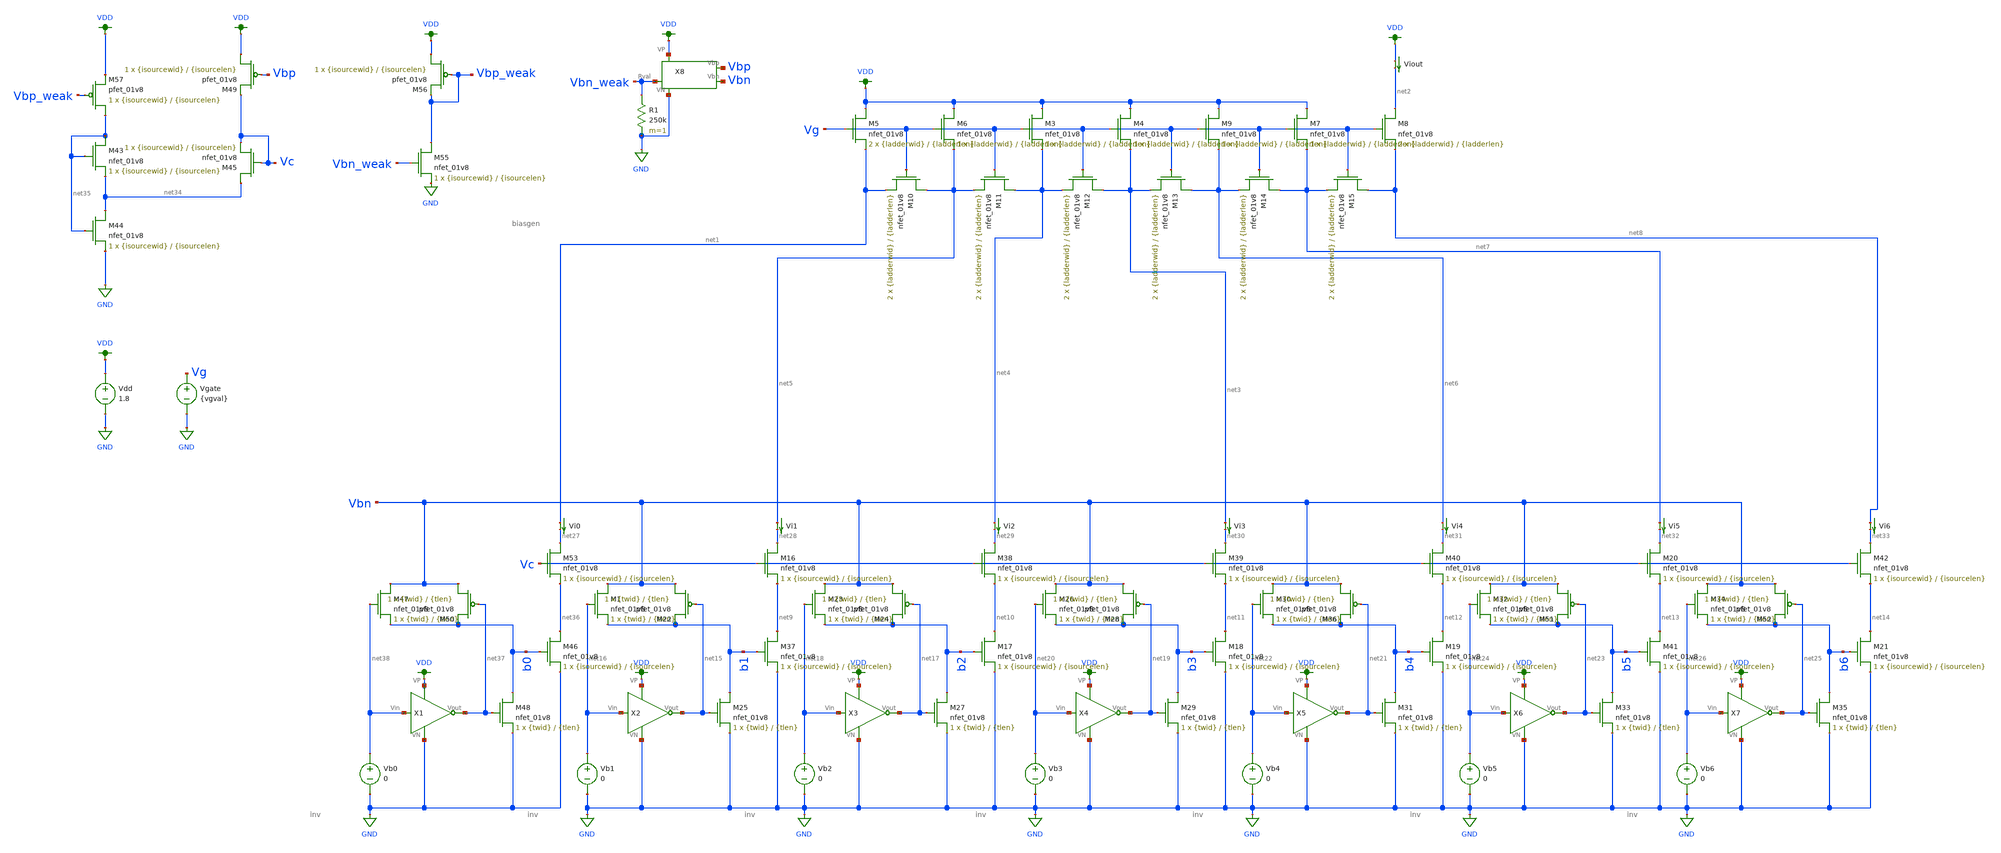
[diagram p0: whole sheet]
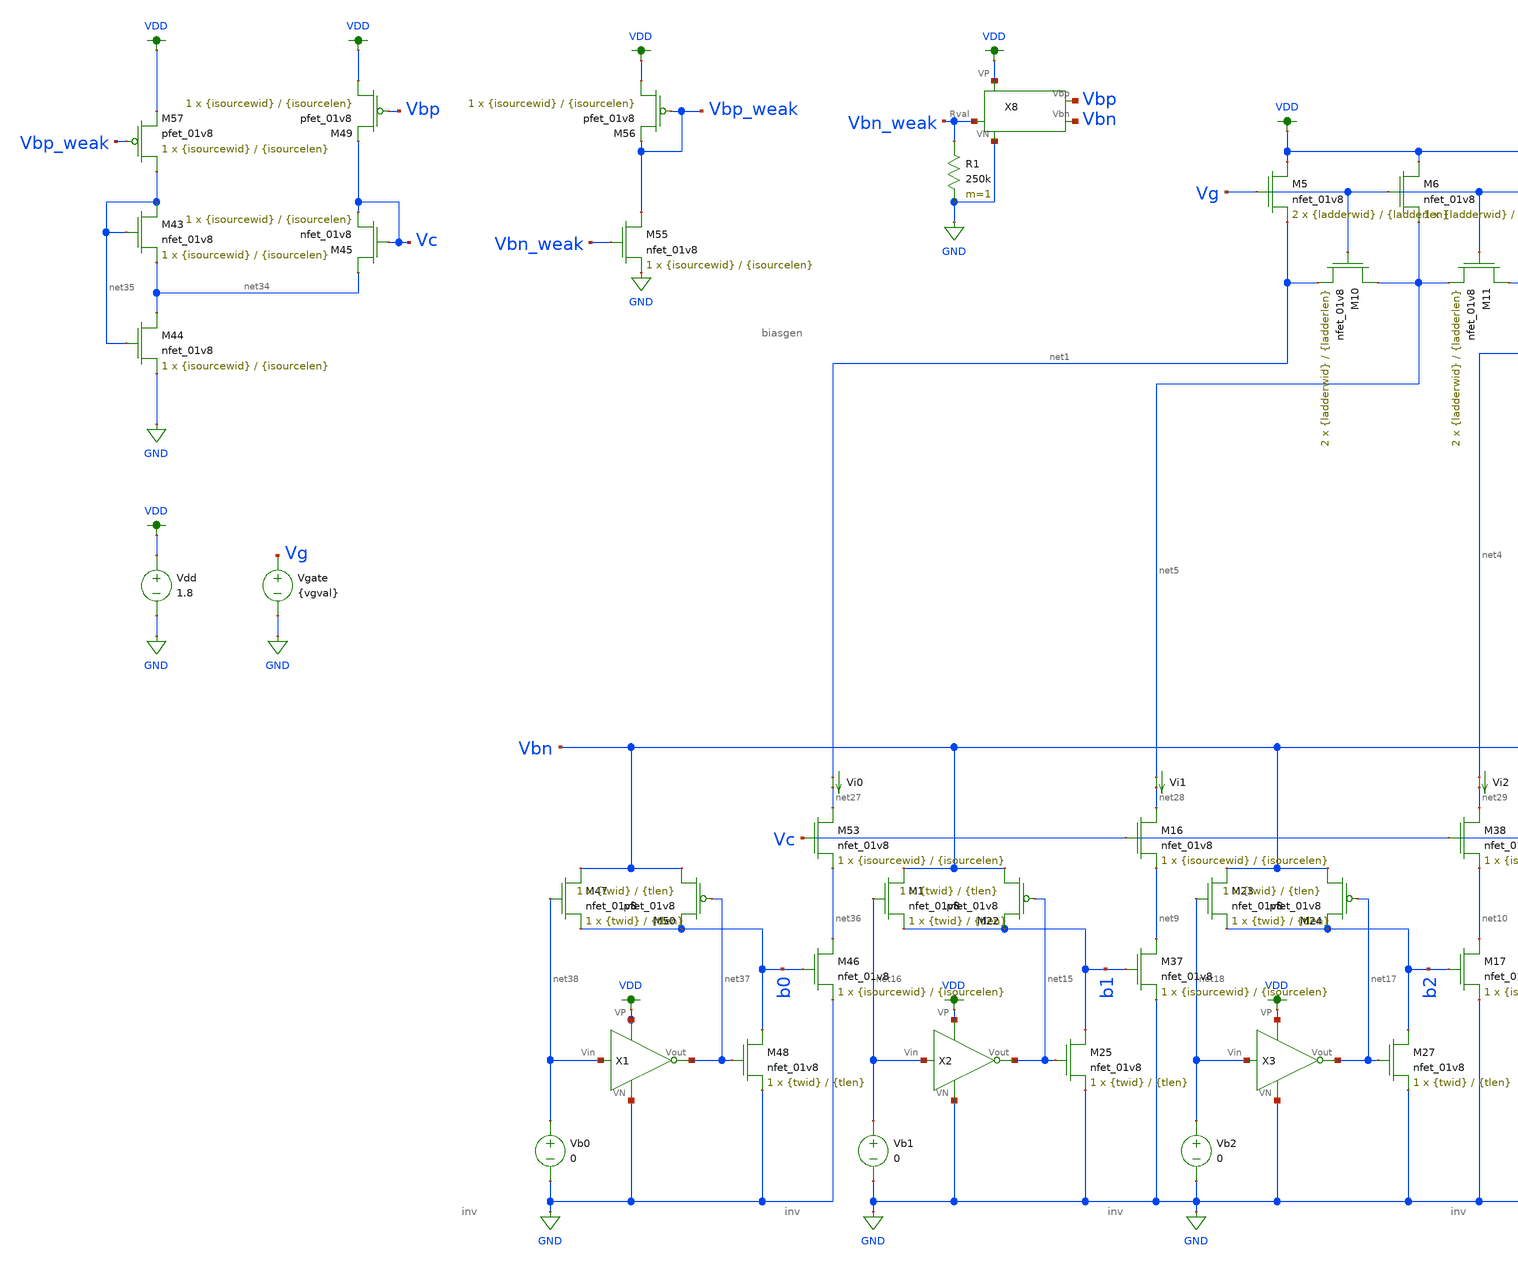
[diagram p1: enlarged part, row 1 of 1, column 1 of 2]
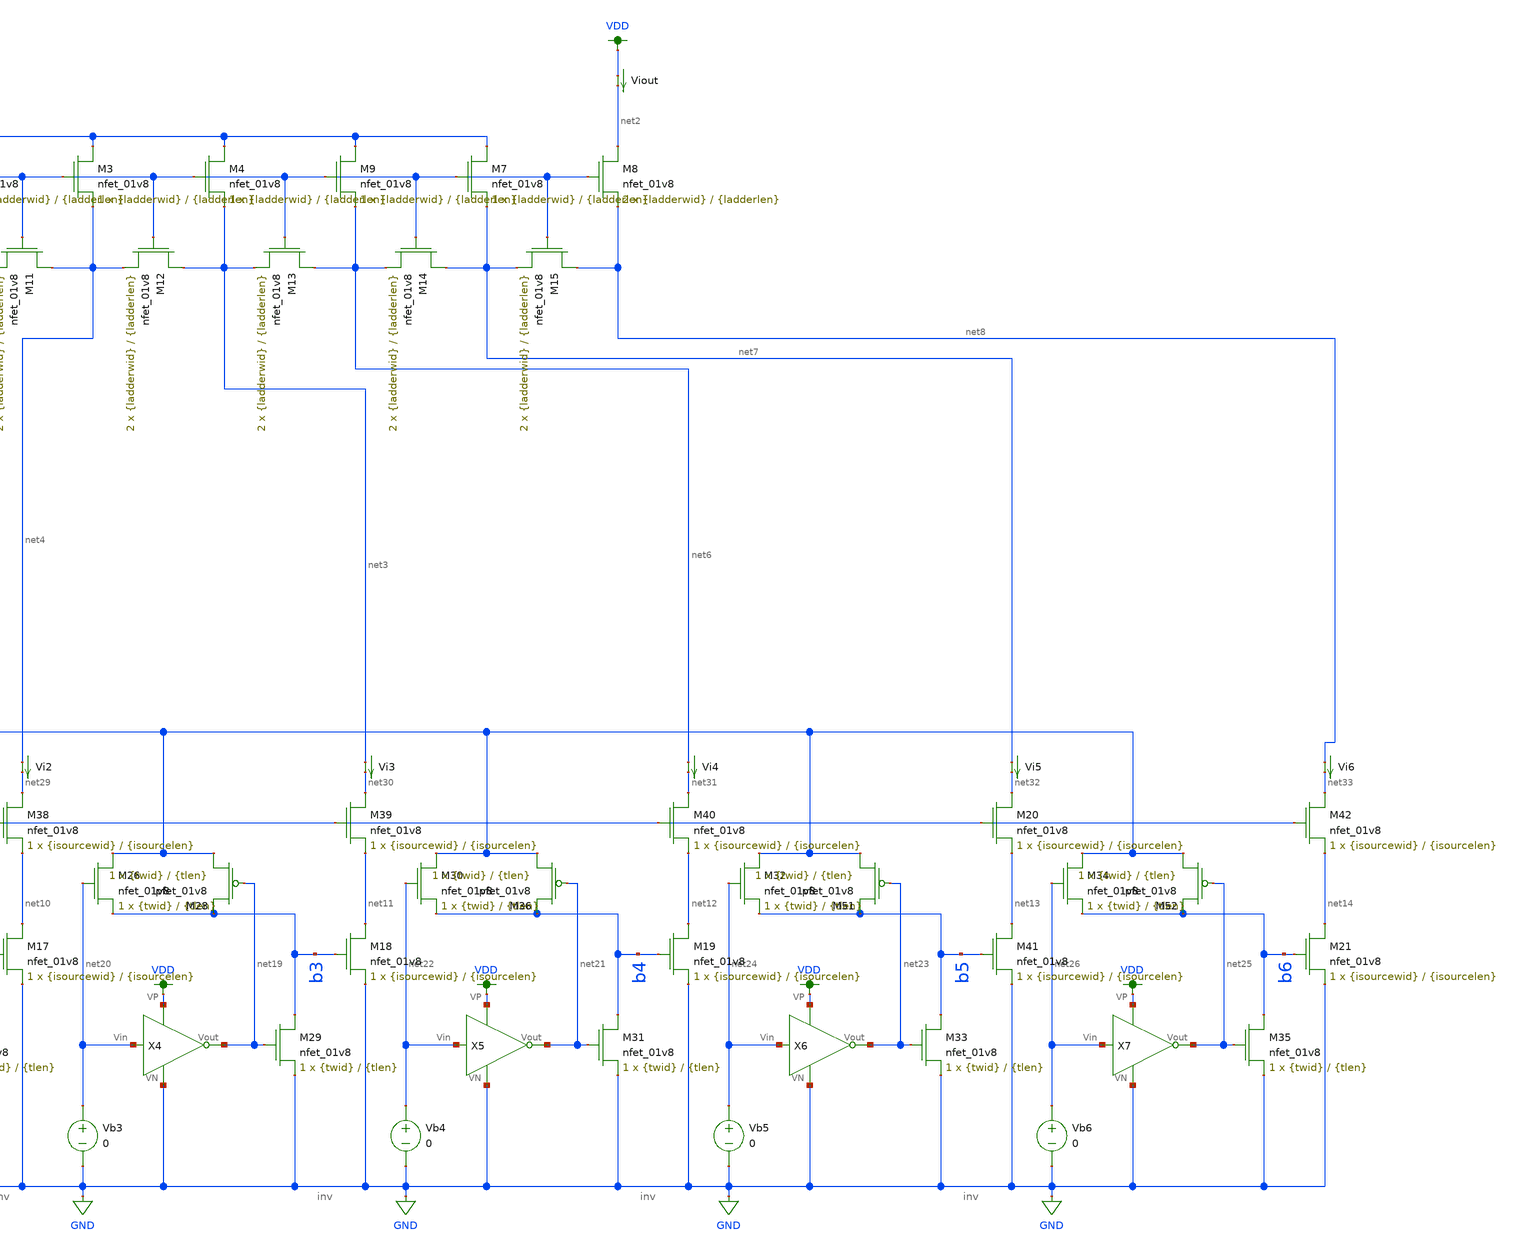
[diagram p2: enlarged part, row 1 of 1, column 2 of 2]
** sch_path: prelim-files/testing.sch
**.subckt testing
Vdd VDD GND 1.8
Vi0 net1 net27 0
.save i(vi0)
XM5 VDD Vg net1 GND sky130_fd_pr__nfet_01v8 L={ladderlen} W={ladderwid} nf=1 ad='int((nf+1)/2) * W/nf * 0.29'
+ as='int((nf+2)/2) * W/nf * 0.29' pd='2*int((nf+1)/2) * (W/nf + 0.29)' ps='2*int((nf+2)/2) * (W/nf + 0.29)'
+ nrd='0.29 / W' nrs='0.29 / W' sa=0 sb=0 sd=0 mult=2 m=2
XM6 VDD Vg net5 GND sky130_fd_pr__nfet_01v8 L={ladderlen} W={ladderwid} nf=1 ad='int((nf+1)/2) * W/nf * 0.29'
+ as='int((nf+2)/2) * W/nf * 0.29' pd='2*int((nf+1)/2) * (W/nf + 0.29)' ps='2*int((nf+2)/2) * (W/nf + 0.29)'
+ nrd='0.29 / W' nrs='0.29 / W' sa=0 sb=0 sd=0 mult=1 m=1
Viout VDD net2 0
.save i(viout)
Vb1 net16 GND 0
Vb2 net18 GND 0
Vgate Vg GND {vgval}
Vi1 net5 net28 0
.save i(vi1)
Vi2 net4 net29 0
.save i(vi2)
Vb3 net20 GND 0
Vi3 net3 net30 0
.save i(vi3)
Vb4 net22 GND 0
Vi4 net6 net31 0
.save i(vi4)
Vb5 net24 GND 0
Vi5 net7 net32 0
.save i(vi5)
Vb6 net26 GND 0
Vi6 net8 net33 0
.save i(vi6)
XM25 b1 net15 GND GND sky130_fd_pr__nfet_01v8 L={tlen} W={twid} nf=1 ad='int((nf+1)/2) * W/nf * 0.29'
+ as='int((nf+2)/2) * W/nf * 0.29' pd='2*int((nf+1)/2) * (W/nf + 0.29)' ps='2*int((nf+2)/2) * (W/nf + 0.29)'
+ nrd='0.29 / W' nrs='0.29 / W' sa=0 sb=0 sd=0 mult=1 m=1
XM27 b2 net17 GND GND sky130_fd_pr__nfet_01v8 L={tlen} W={twid} nf=1 ad='int((nf+1)/2) * W/nf * 0.29'
+ as='int((nf+2)/2) * W/nf * 0.29' pd='2*int((nf+1)/2) * (W/nf + 0.29)' ps='2*int((nf+2)/2) * (W/nf + 0.29)'
+ nrd='0.29 / W' nrs='0.29 / W' sa=0 sb=0 sd=0 mult=1 m=1
XM29 b3 net19 GND GND sky130_fd_pr__nfet_01v8 L={tlen} W={twid} nf=1 ad='int((nf+1)/2) * W/nf * 0.29'
+ as='int((nf+2)/2) * W/nf * 0.29' pd='2*int((nf+1)/2) * (W/nf + 0.29)' ps='2*int((nf+2)/2) * (W/nf + 0.29)'
+ nrd='0.29 / W' nrs='0.29 / W' sa=0 sb=0 sd=0 mult=1 m=1
XM31 b4 net21 GND GND sky130_fd_pr__nfet_01v8 L={tlen} W={twid} nf=1 ad='int((nf+1)/2) * W/nf * 0.29'
+ as='int((nf+2)/2) * W/nf * 0.29' pd='2*int((nf+1)/2) * (W/nf + 0.29)' ps='2*int((nf+2)/2) * (W/nf + 0.29)'
+ nrd='0.29 / W' nrs='0.29 / W' sa=0 sb=0 sd=0 mult=1 m=1
XM33 b5 net23 GND GND sky130_fd_pr__nfet_01v8 L={tlen} W={twid} nf=1 ad='int((nf+1)/2) * W/nf * 0.29'
+ as='int((nf+2)/2) * W/nf * 0.29' pd='2*int((nf+1)/2) * (W/nf + 0.29)' ps='2*int((nf+2)/2) * (W/nf + 0.29)'
+ nrd='0.29 / W' nrs='0.29 / W' sa=0 sb=0 sd=0 mult=1 m=1
XM35 b6 net25 GND GND sky130_fd_pr__nfet_01v8 L={tlen} W={twid} nf=1 ad='int((nf+1)/2) * W/nf * 0.29'
+ as='int((nf+2)/2) * W/nf * 0.29' pd='2*int((nf+1)/2) * (W/nf + 0.29)' ps='2*int((nf+2)/2) * (W/nf + 0.29)'
+ nrd='0.29 / W' nrs='0.29 / W' sa=0 sb=0 sd=0 mult=1 m=1
XM43 net35 net35 net34 GND sky130_fd_pr__nfet_01v8 L={isourcelen} W={isourcewid} nf=1 ad='int((nf+1)/2) * W/nf * 0.29'
+ as='int((nf+2)/2) * W/nf * 0.29' pd='2*int((nf+1)/2) * (W/nf + 0.29)' ps='2*int((nf+2)/2) * (W/nf + 0.29)'
+ nrd='0.29 / W' nrs='0.29 / W' sa=0 sb=0 sd=0 mult=1 m=1
XM44 net34 net35 GND GND sky130_fd_pr__nfet_01v8 L={isourcelen} W={isourcewid} nf=1 ad='int((nf+1)/2) * W/nf * 0.29'
+ as='int((nf+2)/2) * W/nf * 0.29' pd='2*int((nf+1)/2) * (W/nf + 0.29)' ps='2*int((nf+2)/2) * (W/nf + 0.29)'
+ nrd='0.29 / W' nrs='0.29 / W' sa=0 sb=0 sd=0 mult=1 m=1
XM45 net34 Vc Vc GND sky130_fd_pr__nfet_01v8 L={isourcelen} W={isourcewid} nf=1 ad='int((nf+1)/2) * W/nf * 0.29'
+ as='int((nf+2)/2) * W/nf * 0.29' pd='2*int((nf+1)/2) * (W/nf + 0.29)' ps='2*int((nf+2)/2) * (W/nf + 0.29)'
+ nrd='0.29 / W' nrs='0.29 / W' sa=0 sb=0 sd=0 mult=1 m=1
Vb0 net38 GND 0
XM47 Vbn net38 b0 GND sky130_fd_pr__nfet_01v8 L={tlen} W={twid} nf=1 ad='int((nf+1)/2) * W/nf * 0.29'
+ as='int((nf+2)/2) * W/nf * 0.29' pd='2*int((nf+1)/2) * (W/nf + 0.29)' ps='2*int((nf+2)/2) * (W/nf + 0.29)'
+ nrd='0.29 / W' nrs='0.29 / W' sa=0 sb=0 sd=0 mult=1 m=1
XM48 b0 net37 GND GND sky130_fd_pr__nfet_01v8 L={tlen} W={twid} nf=1 ad='int((nf+1)/2) * W/nf * 0.29'
+ as='int((nf+2)/2) * W/nf * 0.29' pd='2*int((nf+1)/2) * (W/nf + 0.29)' ps='2*int((nf+2)/2) * (W/nf + 0.29)'
+ nrd='0.29 / W' nrs='0.29 / W' sa=0 sb=0 sd=0 mult=1 m=1
XM50 Vbn net37 b0 VDD sky130_fd_pr__pfet_01v8 L={tlen} W={twid} nf=1 ad='int((nf+1)/2) * W/nf * 0.29'
+ as='int((nf+2)/2) * W/nf * 0.29' pd='2*int((nf+1)/2) * (W/nf + 0.29)' ps='2*int((nf+2)/2) * (W/nf + 0.29)'
+ nrd='0.29 / W' nrs='0.29 / W' sa=0 sb=0 sd=0 mult=1 m=1
XM1 Vbn net16 b1 GND sky130_fd_pr__nfet_01v8 L={tlen} W={twid} nf=1 ad='int((nf+1)/2) * W/nf * 0.29'
+ as='int((nf+2)/2) * W/nf * 0.29' pd='2*int((nf+1)/2) * (W/nf + 0.29)' ps='2*int((nf+2)/2) * (W/nf + 0.29)'
+ nrd='0.29 / W' nrs='0.29 / W' sa=0 sb=0 sd=0 mult=1 m=1
XM22 Vbn net15 b1 VDD sky130_fd_pr__pfet_01v8 L={tlen} W={twid} nf=1 ad='int((nf+1)/2) * W/nf * 0.29'
+ as='int((nf+2)/2) * W/nf * 0.29' pd='2*int((nf+1)/2) * (W/nf + 0.29)' ps='2*int((nf+2)/2) * (W/nf + 0.29)'
+ nrd='0.29 / W' nrs='0.29 / W' sa=0 sb=0 sd=0 mult=1 m=1
XM23 Vbn net18 b2 GND sky130_fd_pr__nfet_01v8 L={tlen} W={twid} nf=1 ad='int((nf+1)/2) * W/nf * 0.29'
+ as='int((nf+2)/2) * W/nf * 0.29' pd='2*int((nf+1)/2) * (W/nf + 0.29)' ps='2*int((nf+2)/2) * (W/nf + 0.29)'
+ nrd='0.29 / W' nrs='0.29 / W' sa=0 sb=0 sd=0 mult=1 m=1
XM24 Vbn net17 b2 VDD sky130_fd_pr__pfet_01v8 L={tlen} W={twid} nf=1 ad='int((nf+1)/2) * W/nf * 0.29'
+ as='int((nf+2)/2) * W/nf * 0.29' pd='2*int((nf+1)/2) * (W/nf + 0.29)' ps='2*int((nf+2)/2) * (W/nf + 0.29)'
+ nrd='0.29 / W' nrs='0.29 / W' sa=0 sb=0 sd=0 mult=1 m=1
XM26 Vbn net20 b3 GND sky130_fd_pr__nfet_01v8 L={tlen} W={twid} nf=1 ad='int((nf+1)/2) * W/nf * 0.29'
+ as='int((nf+2)/2) * W/nf * 0.29' pd='2*int((nf+1)/2) * (W/nf + 0.29)' ps='2*int((nf+2)/2) * (W/nf + 0.29)'
+ nrd='0.29 / W' nrs='0.29 / W' sa=0 sb=0 sd=0 mult=1 m=1
XM28 Vbn net19 b3 VDD sky130_fd_pr__pfet_01v8 L={tlen} W={twid} nf=1 ad='int((nf+1)/2) * W/nf * 0.29'
+ as='int((nf+2)/2) * W/nf * 0.29' pd='2*int((nf+1)/2) * (W/nf + 0.29)' ps='2*int((nf+2)/2) * (W/nf + 0.29)'
+ nrd='0.29 / W' nrs='0.29 / W' sa=0 sb=0 sd=0 mult=1 m=1
XM30 Vbn net22 b4 GND sky130_fd_pr__nfet_01v8 L={tlen} W={twid} nf=1 ad='int((nf+1)/2) * W/nf * 0.29'
+ as='int((nf+2)/2) * W/nf * 0.29' pd='2*int((nf+1)/2) * (W/nf + 0.29)' ps='2*int((nf+2)/2) * (W/nf + 0.29)'
+ nrd='0.29 / W' nrs='0.29 / W' sa=0 sb=0 sd=0 mult=1 m=1
XM36 Vbn net21 b4 VDD sky130_fd_pr__pfet_01v8 L={tlen} W={twid} nf=1 ad='int((nf+1)/2) * W/nf * 0.29'
+ as='int((nf+2)/2) * W/nf * 0.29' pd='2*int((nf+1)/2) * (W/nf + 0.29)' ps='2*int((nf+2)/2) * (W/nf + 0.29)'
+ nrd='0.29 / W' nrs='0.29 / W' sa=0 sb=0 sd=0 mult=1 m=1
XM32 Vbn net24 b5 GND sky130_fd_pr__nfet_01v8 L={tlen} W={twid} nf=1 ad='int((nf+1)/2) * W/nf * 0.29'
+ as='int((nf+2)/2) * W/nf * 0.29' pd='2*int((nf+1)/2) * (W/nf + 0.29)' ps='2*int((nf+2)/2) * (W/nf + 0.29)'
+ nrd='0.29 / W' nrs='0.29 / W' sa=0 sb=0 sd=0 mult=1 m=1
XM51 Vbn net23 b5 VDD sky130_fd_pr__pfet_01v8 L={tlen} W={twid} nf=1 ad='int((nf+1)/2) * W/nf * 0.29'
+ as='int((nf+2)/2) * W/nf * 0.29' pd='2*int((nf+1)/2) * (W/nf + 0.29)' ps='2*int((nf+2)/2) * (W/nf + 0.29)'
+ nrd='0.29 / W' nrs='0.29 / W' sa=0 sb=0 sd=0 mult=1 m=1
XM34 Vbn net26 b6 GND sky130_fd_pr__nfet_01v8 L={tlen} W={twid} nf=1 ad='int((nf+1)/2) * W/nf * 0.29'
+ as='int((nf+2)/2) * W/nf * 0.29' pd='2*int((nf+1)/2) * (W/nf + 0.29)' ps='2*int((nf+2)/2) * (W/nf + 0.29)'
+ nrd='0.29 / W' nrs='0.29 / W' sa=0 sb=0 sd=0 mult=1 m=1
XM52 Vbn net25 b6 VDD sky130_fd_pr__pfet_01v8 L={tlen} W={twid} nf=1 ad='int((nf+1)/2) * W/nf * 0.29'
+ as='int((nf+2)/2) * W/nf * 0.29' pd='2*int((nf+1)/2) * (W/nf + 0.29)' ps='2*int((nf+2)/2) * (W/nf + 0.29)'
+ nrd='0.29 / W' nrs='0.29 / W' sa=0 sb=0 sd=0 mult=1 m=1
XM10 net5 Vg net1 GND sky130_fd_pr__nfet_01v8 L={ladderlen} W={ladderwid} nf=1 ad='int((nf+1)/2) * W/nf * 0.29'
+ as='int((nf+2)/2) * W/nf * 0.29' pd='2*int((nf+1)/2) * (W/nf + 0.29)' ps='2*int((nf+2)/2) * (W/nf + 0.29)'
+ nrd='0.29 / W' nrs='0.29 / W' sa=0 sb=0 sd=0 mult=2 m=2
XM11 net4 Vg net5 GND sky130_fd_pr__nfet_01v8 L={ladderlen} W={ladderwid} nf=1 ad='int((nf+1)/2) * W/nf * 0.29'
+ as='int((nf+2)/2) * W/nf * 0.29' pd='2*int((nf+1)/2) * (W/nf + 0.29)' ps='2*int((nf+2)/2) * (W/nf + 0.29)'
+ nrd='0.29 / W' nrs='0.29 / W' sa=0 sb=0 sd=0 mult=2 m=2
XM12 net3 Vg net4 GND sky130_fd_pr__nfet_01v8 L={ladderlen} W={ladderwid} nf=1 ad='int((nf+1)/2) * W/nf * 0.29'
+ as='int((nf+2)/2) * W/nf * 0.29' pd='2*int((nf+1)/2) * (W/nf + 0.29)' ps='2*int((nf+2)/2) * (W/nf + 0.29)'
+ nrd='0.29 / W' nrs='0.29 / W' sa=0 sb=0 sd=0 mult=2 m=2
XM13 net6 Vg net3 GND sky130_fd_pr__nfet_01v8 L={ladderlen} W={ladderwid} nf=1 ad='int((nf+1)/2) * W/nf * 0.29'
+ as='int((nf+2)/2) * W/nf * 0.29' pd='2*int((nf+1)/2) * (W/nf + 0.29)' ps='2*int((nf+2)/2) * (W/nf + 0.29)'
+ nrd='0.29 / W' nrs='0.29 / W' sa=0 sb=0 sd=0 mult=2 m=2
XM14 net7 Vg net6 GND sky130_fd_pr__nfet_01v8 L={ladderlen} W={ladderwid} nf=1 ad='int((nf+1)/2) * W/nf * 0.29'
+ as='int((nf+2)/2) * W/nf * 0.29' pd='2*int((nf+1)/2) * (W/nf + 0.29)' ps='2*int((nf+2)/2) * (W/nf + 0.29)'
+ nrd='0.29 / W' nrs='0.29 / W' sa=0 sb=0 sd=0 mult=2 m=2
XM15 net8 Vg net7 GND sky130_fd_pr__nfet_01v8 L={ladderlen} W={ladderwid} nf=1 ad='int((nf+1)/2) * W/nf * 0.29'
+ as='int((nf+2)/2) * W/nf * 0.29' pd='2*int((nf+1)/2) * (W/nf + 0.29)' ps='2*int((nf+2)/2) * (W/nf + 0.29)'
+ nrd='0.29 / W' nrs='0.29 / W' sa=0 sb=0 sd=0 mult=2 m=2
XM8 net2 Vg net8 GND sky130_fd_pr__nfet_01v8 L={ladderlen} W={ladderwid} nf=1 ad='int((nf+1)/2) * W/nf * 0.29'
+ as='int((nf+2)/2) * W/nf * 0.29' pd='2*int((nf+1)/2) * (W/nf + 0.29)' ps='2*int((nf+2)/2) * (W/nf + 0.29)'
+ nrd='0.29 / W' nrs='0.29 / W' sa=0 sb=0 sd=0 mult=2 m=2
XM3 VDD Vg net4 GND sky130_fd_pr__nfet_01v8 L={ladderlen} W={ladderwid} nf=1 ad='int((nf+1)/2) * W/nf * 0.29'
+ as='int((nf+2)/2) * W/nf * 0.29' pd='2*int((nf+1)/2) * (W/nf + 0.29)' ps='2*int((nf+2)/2) * (W/nf + 0.29)'
+ nrd='0.29 / W' nrs='0.29 / W' sa=0 sb=0 sd=0 mult=1 m=1
XM4 VDD Vg net3 GND sky130_fd_pr__nfet_01v8 L={ladderlen} W={ladderwid} nf=1 ad='int((nf+1)/2) * W/nf * 0.29'
+ as='int((nf+2)/2) * W/nf * 0.29' pd='2*int((nf+1)/2) * (W/nf + 0.29)' ps='2*int((nf+2)/2) * (W/nf + 0.29)'
+ nrd='0.29 / W' nrs='0.29 / W' sa=0 sb=0 sd=0 mult=1 m=1
XM9 VDD Vg net6 GND sky130_fd_pr__nfet_01v8 L={ladderlen} W={ladderwid} nf=1 ad='int((nf+1)/2) * W/nf * 0.29'
+ as='int((nf+2)/2) * W/nf * 0.29' pd='2*int((nf+1)/2) * (W/nf + 0.29)' ps='2*int((nf+2)/2) * (W/nf + 0.29)'
+ nrd='0.29 / W' nrs='0.29 / W' sa=0 sb=0 sd=0 mult=1 m=1
XM7 VDD Vg net7 GND sky130_fd_pr__nfet_01v8 L={ladderlen} W={ladderwid} nf=1 ad='int((nf+1)/2) * W/nf * 0.29'
+ as='int((nf+2)/2) * W/nf * 0.29' pd='2*int((nf+1)/2) * (W/nf + 0.29)' ps='2*int((nf+2)/2) * (W/nf + 0.29)'
+ nrd='0.29 / W' nrs='0.29 / W' sa=0 sb=0 sd=0 mult=1 m=1
XM53 net27 Vc net36 GND sky130_fd_pr__nfet_01v8 L={isourcelen} W={isourcewid} nf=1 ad='int((nf+1)/2) * W/nf * 0.29'
+ as='int((nf+2)/2) * W/nf * 0.29' pd='2*int((nf+1)/2) * (W/nf + 0.29)' ps='2*int((nf+2)/2) * (W/nf + 0.29)'
+ nrd='0.29 / W' nrs='0.29 / W' sa=0 sb=0 sd=0 mult=1 m=1
XM46 net36 b0 GND GND sky130_fd_pr__nfet_01v8 L={isourcelen} W={isourcewid} nf=1 ad='int((nf+1)/2) * W/nf * 0.29'
+ as='int((nf+2)/2) * W/nf * 0.29' pd='2*int((nf+1)/2) * (W/nf + 0.29)' ps='2*int((nf+2)/2) * (W/nf + 0.29)'
+ nrd='0.29 / W' nrs='0.29 / W' sa=0 sb=0 sd=0 mult=1 m=1
XM37 net9 b1 GND GND sky130_fd_pr__nfet_01v8 L={isourcelen} W={isourcewid} nf=1 ad='int((nf+1)/2) * W/nf * 0.29'
+ as='int((nf+2)/2) * W/nf * 0.29' pd='2*int((nf+1)/2) * (W/nf + 0.29)' ps='2*int((nf+2)/2) * (W/nf + 0.29)'
+ nrd='0.29 / W' nrs='0.29 / W' sa=0 sb=0 sd=0 mult=1 m=1
XM16 net28 Vc net9 GND sky130_fd_pr__nfet_01v8 L={isourcelen} W={isourcewid} nf=1 ad='int((nf+1)/2) * W/nf * 0.29'
+ as='int((nf+2)/2) * W/nf * 0.29' pd='2*int((nf+1)/2) * (W/nf + 0.29)' ps='2*int((nf+2)/2) * (W/nf + 0.29)'
+ nrd='0.29 / W' nrs='0.29 / W' sa=0 sb=0 sd=0 mult=1 m=1
XM17 net10 b2 GND GND sky130_fd_pr__nfet_01v8 L={isourcelen} W={isourcewid} nf=1 ad='int((nf+1)/2) * W/nf * 0.29'
+ as='int((nf+2)/2) * W/nf * 0.29' pd='2*int((nf+1)/2) * (W/nf + 0.29)' ps='2*int((nf+2)/2) * (W/nf + 0.29)'
+ nrd='0.29 / W' nrs='0.29 / W' sa=0 sb=0 sd=0 mult=1 m=1
XM38 net29 Vc net10 GND sky130_fd_pr__nfet_01v8 L={isourcelen} W={isourcewid} nf=1 ad='int((nf+1)/2) * W/nf * 0.29'
+ as='int((nf+2)/2) * W/nf * 0.29' pd='2*int((nf+1)/2) * (W/nf + 0.29)' ps='2*int((nf+2)/2) * (W/nf + 0.29)'
+ nrd='0.29 / W' nrs='0.29 / W' sa=0 sb=0 sd=0 mult=1 m=1
XM18 net11 b3 GND GND sky130_fd_pr__nfet_01v8 L={isourcelen} W={isourcewid} nf=1 ad='int((nf+1)/2) * W/nf * 0.29'
+ as='int((nf+2)/2) * W/nf * 0.29' pd='2*int((nf+1)/2) * (W/nf + 0.29)' ps='2*int((nf+2)/2) * (W/nf + 0.29)'
+ nrd='0.29 / W' nrs='0.29 / W' sa=0 sb=0 sd=0 mult=1 m=1
XM39 net30 Vc net11 GND sky130_fd_pr__nfet_01v8 L={isourcelen} W={isourcewid} nf=1 ad='int((nf+1)/2) * W/nf * 0.29'
+ as='int((nf+2)/2) * W/nf * 0.29' pd='2*int((nf+1)/2) * (W/nf + 0.29)' ps='2*int((nf+2)/2) * (W/nf + 0.29)'
+ nrd='0.29 / W' nrs='0.29 / W' sa=0 sb=0 sd=0 mult=1 m=1
XM19 net12 b4 GND GND sky130_fd_pr__nfet_01v8 L={isourcelen} W={isourcewid} nf=1 ad='int((nf+1)/2) * W/nf * 0.29'
+ as='int((nf+2)/2) * W/nf * 0.29' pd='2*int((nf+1)/2) * (W/nf + 0.29)' ps='2*int((nf+2)/2) * (W/nf + 0.29)'
+ nrd='0.29 / W' nrs='0.29 / W' sa=0 sb=0 sd=0 mult=1 m=1
XM40 net31 Vc net12 GND sky130_fd_pr__nfet_01v8 L={isourcelen} W={isourcewid} nf=1 ad='int((nf+1)/2) * W/nf * 0.29'
+ as='int((nf+2)/2) * W/nf * 0.29' pd='2*int((nf+1)/2) * (W/nf + 0.29)' ps='2*int((nf+2)/2) * (W/nf + 0.29)'
+ nrd='0.29 / W' nrs='0.29 / W' sa=0 sb=0 sd=0 mult=1 m=1
XM20 net32 Vc net13 GND sky130_fd_pr__nfet_01v8 L={isourcelen} W={isourcewid} nf=1 ad='int((nf+1)/2) * W/nf * 0.29'
+ as='int((nf+2)/2) * W/nf * 0.29' pd='2*int((nf+1)/2) * (W/nf + 0.29)' ps='2*int((nf+2)/2) * (W/nf + 0.29)'
+ nrd='0.29 / W' nrs='0.29 / W' sa=0 sb=0 sd=0 mult=1 m=1
XM41 net13 b5 GND GND sky130_fd_pr__nfet_01v8 L={isourcelen} W={isourcewid} nf=1 ad='int((nf+1)/2) * W/nf * 0.29'
+ as='int((nf+2)/2) * W/nf * 0.29' pd='2*int((nf+1)/2) * (W/nf + 0.29)' ps='2*int((nf+2)/2) * (W/nf + 0.29)'
+ nrd='0.29 / W' nrs='0.29 / W' sa=0 sb=0 sd=0 mult=1 m=1
XM21 net14 b6 GND GND sky130_fd_pr__nfet_01v8 L={isourcelen} W={isourcewid} nf=1 ad='int((nf+1)/2) * W/nf * 0.29'
+ as='int((nf+2)/2) * W/nf * 0.29' pd='2*int((nf+1)/2) * (W/nf + 0.29)' ps='2*int((nf+2)/2) * (W/nf + 0.29)'
+ nrd='0.29 / W' nrs='0.29 / W' sa=0 sb=0 sd=0 mult=1 m=1
XM42 net33 Vc net14 GND sky130_fd_pr__nfet_01v8 L={isourcelen} W={isourcewid} nf=1 ad='int((nf+1)/2) * W/nf * 0.29'
+ as='int((nf+2)/2) * W/nf * 0.29' pd='2*int((nf+1)/2) * (W/nf + 0.29)' ps='2*int((nf+2)/2) * (W/nf + 0.29)'
+ nrd='0.29 / W' nrs='0.29 / W' sa=0 sb=0 sd=0 mult=1 m=1
R1 Vbn_weak GND 250k m=1
XM49 VDD Vbp Vc VDD sky130_fd_pr__pfet_01v8 L={isourcelen} W={isourcewid} nf=1 ad='int((nf+1)/2) * W/nf * 0.29'
+ as='int((nf+2)/2) * W/nf * 0.29' pd='2*int((nf+1)/2) * (W/nf + 0.29)' ps='2*int((nf+2)/2) * (W/nf + 0.29)'
+ nrd='0.29 / W' nrs='0.29 / W' sa=0 sb=0 sd=0 mult=1 m=1
XM55 Vbp_weak Vbn_weak GND GND sky130_fd_pr__nfet_01v8 L={isourcelen} W={isourcewid} nf=1 ad='int((nf+1)/2) * W/nf * 0.29'
+ as='int((nf+2)/2) * W/nf * 0.29' pd='2*int((nf+1)/2) * (W/nf + 0.29)' ps='2*int((nf+2)/2) * (W/nf + 0.29)'
+ nrd='0.29 / W' nrs='0.29 / W' sa=0 sb=0 sd=0 mult=1 m=1
XM56 VDD Vbp_weak Vbp_weak VDD sky130_fd_pr__pfet_01v8 L={isourcelen} W={isourcewid} nf=1 ad='int((nf+1)/2) * W/nf * 0.29'
+ as='int((nf+2)/2) * W/nf * 0.29' pd='2*int((nf+1)/2) * (W/nf + 0.29)' ps='2*int((nf+2)/2) * (W/nf + 0.29)'
+ nrd='0.29 / W' nrs='0.29 / W' sa=0 sb=0 sd=0 mult=1 m=1
XM57 net35 Vbp_weak VDD VDD sky130_fd_pr__pfet_01v8 L={isourcelen} W={isourcewid} nf=1 ad='int((nf+1)/2) * W/nf * 0.29'
+ as='int((nf+2)/2) * W/nf * 0.29' pd='2*int((nf+1)/2) * (W/nf + 0.29)' ps='2*int((nf+2)/2) * (W/nf + 0.29)'
+ nrd='0.29 / W' nrs='0.29 / W' sa=0 sb=0 sd=0 mult=1 m=1
X8 Vbn_weak GND VDD Vbp Vbn biasgen
X1 net38 net37 VDD GND inv
X2 net16 net15 VDD GND inv
X3 net18 net17 VDD GND inv
X4 net20 net19 VDD GND inv
X5 net22 net21 VDD GND inv
X6 net24 net23 VDD GND inv
X7 net26 net25 VDD GND inv
**** begin user architecture code

.option wnflag=1
.param MC_SWITCH=0.0
.lib ~/skywater/skywater-pdk/libraries/sky130_fd_pr_ngspice/latest/models/sky130.lib.spice tt


.param M=8
.param vgval=1.8
.param tlen=0.3
.param twid=3.15
.param ladderlen=1.4
.param ladderwid=5.7
.param isourcelen=0.5
.param isourcewid=1.4
.control
	set wr_vecnames
	set wr_singlescale
	let code = 0
	while code < 128
		if code eq 0
			let nb0 = 0
		else
			let nb0 = (code % 2)*1.8
		end
		if floor(code / 2) eq 0
			let nb1 = 0
		else
			let nb1 = (floor(code / 2) % 2)*1.8
		end
		if floor(code / 4) eq 0
			let nb2 = 0
		else
			let nb2 = (floor(code / 4) % 2)*1.8
		end
		if floor(code / 8) eq 0
			let nb3 = 0
		else
			let nb3 = (floor(code / 8) % 2)*1.8
		end
		if floor(code / 16) eq 0
			let nb4 = 0
		else
			let nb4 = (floor(code / 16) % 2)*1.8
		end
		if floor(code / 32) eq 0
			let nb5 = 0
		else
			let nb5 = (floor(code / 32) % 2)*1.8
		end
		if floor(code / 64) eq 0
			let nb6 = 0
		else
			let nb6 = (floor(code / 64) % 2)*1.8
		end
		alter Vb0 $&nb0
		alter Vb1 $&nb1
		alter Vb2 $&nb2
		alter Vb3 $&nb3
		alter Vb4 $&nb4
		alter Vb5 $&nb5
		alter Vb6 $&nb6
		save all
		op
		wrdata ~/VLSI/MP4/VLSI-MP4/prelim-files/dacdata.txt i(Viout)
		if code eq 0
			set appendwrite
			set wr_vecnames = FALSE
		end
		let code = code + 1
	end
	quit
.endc

**** end user architecture code
**.ends

* expanding   symbol:  /home/jonah/VLSI/VLSI-MP4/prelim-files/biasgen.sym # of pins=5
** sym_path: prelim-files/biasgen.sym
** sch_path: prelim-files/biasgen.sch
.subckt biasgen Rval VN VP Vbp Vbn
*.iopin Rval
*.iopin VN
*.iopin VP
*.iopin Vbp
*.iopin Vbn
XM1 net1 net2 VN GND sky130_fd_pr__nfet_01v8 L={isourcelen} W={isourcewid} nf=1 ad='int((nf+1)/2) * W/nf * 0.29'
+ as='int((nf+2)/2) * W/nf * 0.29' pd='2*int((nf+1)/2) * (W/nf + 0.29)' ps='2*int((nf+2)/2) * (W/nf + 0.29)'
+ nrd='0.29 / W' nrs='0.29 / W' sa=0 sb=0 sd=0 mult=1 m=1
XM5 Rval net2 net2 GND sky130_fd_pr__nfet_01v8 L={isourcelen} W={isourcewid} nf=1 ad='int((nf+1)/2) * W/nf * 0.29'
+ as='int((nf+2)/2) * W/nf * 0.29' pd='2*int((nf+1)/2) * (W/nf + 0.29)' ps='2*int((nf+2)/2) * (W/nf + 0.29)'
+ nrd='0.29 / W' nrs='0.29 / W' sa=0 sb=0 sd=0 mult={M} m={M}
Viout net3 Vbn 0
.save i(viout)
XM8 VP Vbp net2 VDD sky130_fd_pr__pfet_01v8 L={isourcelen} W={isourcewid} nf=1 ad='int((nf+1)/2) * W/nf * 0.29'
+ as='int((nf+2)/2) * W/nf * 0.29' pd='2*int((nf+1)/2) * (W/nf + 0.29)' ps='2*int((nf+2)/2) * (W/nf + 0.29)'
+ nrd='0.29 / W' nrs='0.29 / W' sa=0 sb=0 sd=0 mult=1 m=1
XM3 VP net1 net1 VDD sky130_fd_pr__pfet_01v8 L={isourcelen} W={isourcewid} nf=1 ad='int((nf+1)/2) * W/nf * 0.29'
+ as='int((nf+2)/2) * W/nf * 0.29' pd='2*int((nf+1)/2) * (W/nf + 0.29)' ps='2*int((nf+2)/2) * (W/nf + 0.29)'
+ nrd='0.29 / W' nrs='0.29 / W' sa=0 sb=0 sd=0 mult=1 m=1
XM2 Vbp net1 VP VDD sky130_fd_pr__pfet_01v8 L={isourcelen} W={isourcewid} nf=1 ad='int((nf+1)/2) * W/nf * 0.29'
+ as='int((nf+2)/2) * W/nf * 0.29' pd='2*int((nf+1)/2) * (W/nf + 0.29)' ps='2*int((nf+2)/2) * (W/nf + 0.29)'
+ nrd='0.29 / W' nrs='0.29 / W' sa=0 sb=0 sd=0 mult=1 m=1
XM7 net3 Vbp VP VDD sky130_fd_pr__pfet_01v8 L={isourcelen} W={isourcewid} nf=1 ad='int((nf+1)/2) * W/nf * 0.29'
+ as='int((nf+2)/2) * W/nf * 0.29' pd='2*int((nf+1)/2) * (W/nf + 0.29)' ps='2*int((nf+2)/2) * (W/nf + 0.29)'
+ nrd='0.29 / W' nrs='0.29 / W' sa=0 sb=0 sd=0 mult=1 m=1
XM4 VN Vbn Vbp GND sky130_fd_pr__nfet_01v8 L={isourcelen} W={isourcewid} nf=1 ad='int((nf+1)/2) * W/nf * 0.29'
+ as='int((nf+2)/2) * W/nf * 0.29' pd='2*int((nf+1)/2) * (W/nf + 0.29)' ps='2*int((nf+2)/2) * (W/nf + 0.29)'
+ nrd='0.29 / W' nrs='0.29 / W' sa=0 sb=0 sd=0 mult=1 m=1
XM6 Vbn Vbn VN GND sky130_fd_pr__nfet_01v8 L={isourcelen} W={isourcewid} nf=1 ad='int((nf+1)/2) * W/nf * 0.29'
+ as='int((nf+2)/2) * W/nf * 0.29' pd='2*int((nf+1)/2) * (W/nf + 0.29)' ps='2*int((nf+2)/2) * (W/nf + 0.29)'
+ nrd='0.29 / W' nrs='0.29 / W' sa=0 sb=0 sd=0 mult=1 m=1
.ends


* expanding   symbol:  /home/jonah/VLSI/VLSI-MP4/prelim-files/inv.sym # of pins=4
** sym_path: prelim-files/inv.sym
** sch_path: prelim-files/inv.sch
.subckt inv Vin Vout VP VN
*.iopin VP
*.iopin VN
*.ipin Vin
*.iopin Vout
XM1 Vout Vin VN GND sky130_fd_pr__nfet_01v8 L={tlen} W={twid} nf=1 ad='int((nf+1)/2) * W/nf * 0.29' as='int((nf+2)/2) * W/nf * 0.29'
+ pd='2*int((nf+1)/2) * (W/nf + 0.29)' ps='2*int((nf+2)/2) * (W/nf + 0.29)' nrd='0.29 / W' nrs='0.29 / W'
+ sa=0 sb=0 sd=0 mult=1 m=1
XM2 Vout Vin VP VDD sky130_fd_pr__pfet_01v8 L={tlen} W={twid} nf=1 ad='int((nf+1)/2) * W/nf * 0.29' as='int((nf+2)/2) * W/nf * 0.29'
+ pd='2*int((nf+1)/2) * (W/nf + 0.29)' ps='2*int((nf+2)/2) * (W/nf + 0.29)' nrd='0.29 / W' nrs='0.29 / W'
+ sa=0 sb=0 sd=0 mult=1 m=1
.ends

.GLOBAL GND
.GLOBAL VDD
.end
